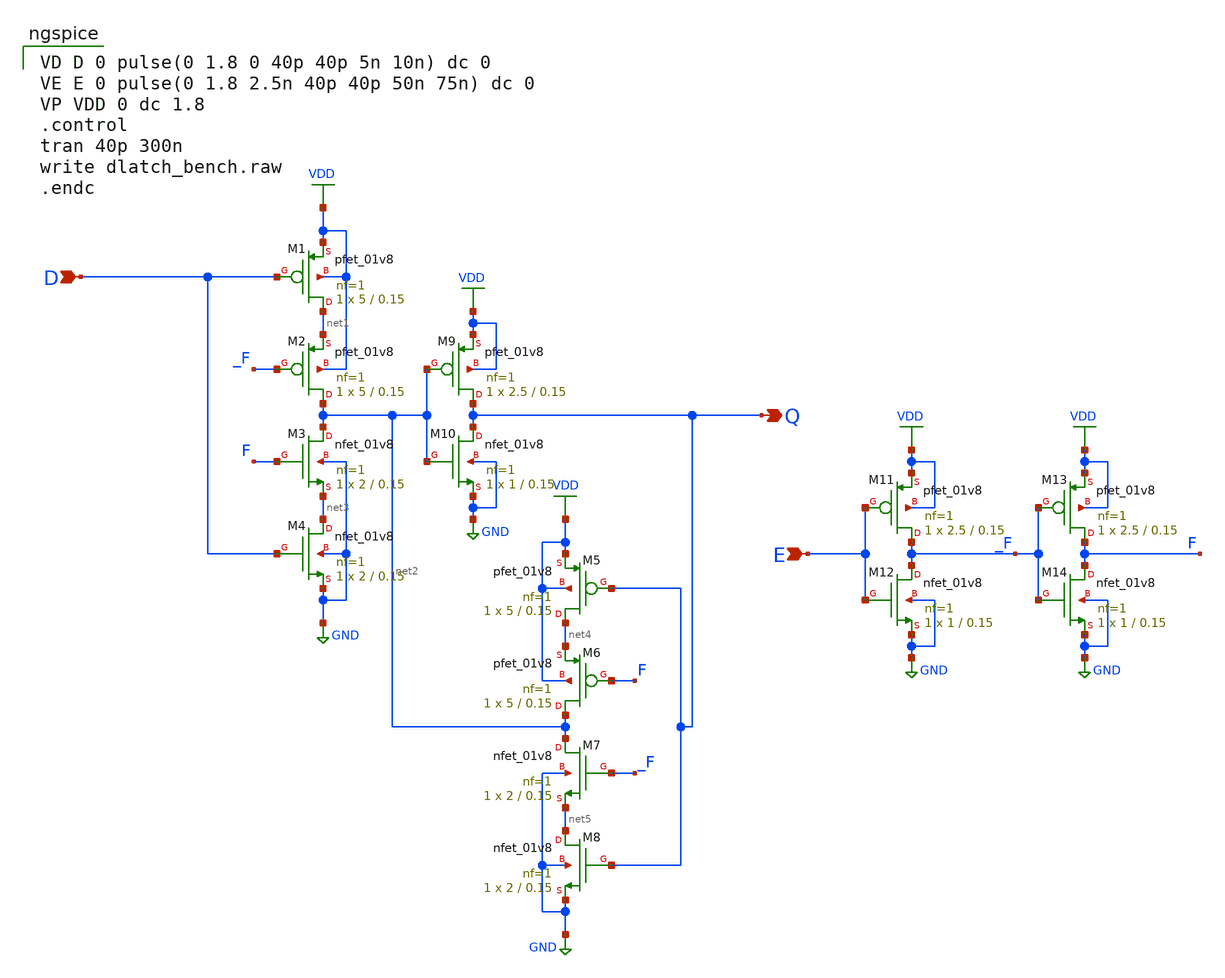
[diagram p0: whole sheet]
** sch_path: dlatch_bench2.sch
**.subckt dlatch_bench2 E D Q
*.ipin E
*.ipin D
*.opin Q
XM1 net1 D VDD VDD sky130_fd_pr__pfet_01v8 L=0.15 W=5 nf=1 ad='int((nf+1)/2) * W/nf * 0.29' as='int((nf+2)/2) * W/nf * 0.29'
+ pd='2*int((nf+1)/2) * (W/nf + 0.29)' ps='2*int((nf+2)/2) * (W/nf + 0.29)' nrd='0.29 / W' nrs='0.29 / W'
+ sa=0 sb=0 sd=0 mult=1 m=1
XM2 net2 _F net1 VDD sky130_fd_pr__pfet_01v8 L=0.15 W=5 nf=1 ad='int((nf+1)/2) * W/nf * 0.29' as='int((nf+2)/2) * W/nf * 0.29'
+ pd='2*int((nf+1)/2) * (W/nf + 0.29)' ps='2*int((nf+2)/2) * (W/nf + 0.29)' nrd='0.29 / W' nrs='0.29 / W'
+ sa=0 sb=0 sd=0 mult=1 m=1
XM3 net2 F net3 GND sky130_fd_pr__nfet_01v8 L=0.15 W=2 nf=1 ad='int((nf+1)/2) * W/nf * 0.29' as='int((nf+2)/2) * W/nf * 0.29'
+ pd='2*int((nf+1)/2) * (W/nf + 0.29)' ps='2*int((nf+2)/2) * (W/nf + 0.29)' nrd='0.29 / W' nrs='0.29 / W'
+ sa=0 sb=0 sd=0 mult=1 m=1
XM4 net3 D GND GND sky130_fd_pr__nfet_01v8 L=0.15 W=2 nf=1 ad='int((nf+1)/2) * W/nf * 0.29' as='int((nf+2)/2) * W/nf * 0.29'
+ pd='2*int((nf+1)/2) * (W/nf + 0.29)' ps='2*int((nf+2)/2) * (W/nf + 0.29)' nrd='0.29 / W' nrs='0.29 / W'
+ sa=0 sb=0 sd=0 mult=1 m=1
XM5 net4 Q VDD VDD sky130_fd_pr__pfet_01v8 L=0.15 W=5 nf=1 ad='int((nf+1)/2) * W/nf * 0.29' as='int((nf+2)/2) * W/nf * 0.29'
+ pd='2*int((nf+1)/2) * (W/nf + 0.29)' ps='2*int((nf+2)/2) * (W/nf + 0.29)' nrd='0.29 / W' nrs='0.29 / W'
+ sa=0 sb=0 sd=0 mult=1 m=1
XM6 net2 F net4 VDD sky130_fd_pr__pfet_01v8 L=0.15 W=5 nf=1 ad='int((nf+1)/2) * W/nf * 0.29' as='int((nf+2)/2) * W/nf * 0.29'
+ pd='2*int((nf+1)/2) * (W/nf + 0.29)' ps='2*int((nf+2)/2) * (W/nf + 0.29)' nrd='0.29 / W' nrs='0.29 / W'
+ sa=0 sb=0 sd=0 mult=1 m=1
XM7 net2 _F net5 GND sky130_fd_pr__nfet_01v8 L=0.15 W=2 nf=1 ad='int((nf+1)/2) * W/nf * 0.29' as='int((nf+2)/2) * W/nf * 0.29'
+ pd='2*int((nf+1)/2) * (W/nf + 0.29)' ps='2*int((nf+2)/2) * (W/nf + 0.29)' nrd='0.29 / W' nrs='0.29 / W'
+ sa=0 sb=0 sd=0 mult=1 m=1
XM8 net5 Q GND GND sky130_fd_pr__nfet_01v8 L=0.15 W=2 nf=1 ad='int((nf+1)/2) * W/nf * 0.29' as='int((nf+2)/2) * W/nf * 0.29'
+ pd='2*int((nf+1)/2) * (W/nf + 0.29)' ps='2*int((nf+2)/2) * (W/nf + 0.29)' nrd='0.29 / W' nrs='0.29 / W'
+ sa=0 sb=0 sd=0 mult=1 m=1
XM9 Q net2 VDD VDD sky130_fd_pr__pfet_01v8 L=0.15 W=2.5 nf=1 ad='int((nf+1)/2) * W/nf * 0.29' as='int((nf+2)/2) * W/nf * 0.29'
+ pd='2*int((nf+1)/2) * (W/nf + 0.29)' ps='2*int((nf+2)/2) * (W/nf + 0.29)' nrd='0.29 / W' nrs='0.29 / W'
+ sa=0 sb=0 sd=0 mult=1 m=1
XM10 Q net2 GND GND sky130_fd_pr__nfet_01v8 L=0.15 W=1 nf=1 ad='int((nf+1)/2) * W/nf * 0.29' as='int((nf+2)/2) * W/nf * 0.29'
+ pd='2*int((nf+1)/2) * (W/nf + 0.29)' ps='2*int((nf+2)/2) * (W/nf + 0.29)' nrd='0.29 / W' nrs='0.29 / W'
+ sa=0 sb=0 sd=0 mult=1 m=1
XM11 _F E VDD VDD sky130_fd_pr__pfet_01v8 L=0.15 W=2.5 nf=1 ad='int((nf+1)/2) * W/nf * 0.29' as='int((nf+2)/2) * W/nf * 0.29'
+ pd='2*int((nf+1)/2) * (W/nf + 0.29)' ps='2*int((nf+2)/2) * (W/nf + 0.29)' nrd='0.29 / W' nrs='0.29 / W'
+ sa=0 sb=0 sd=0 mult=1 m=1
XM12 _F E GND GND sky130_fd_pr__nfet_01v8 L=0.15 W=1 nf=1 ad='int((nf+1)/2) * W/nf * 0.29' as='int((nf+2)/2) * W/nf * 0.29'
+ pd='2*int((nf+1)/2) * (W/nf + 0.29)' ps='2*int((nf+2)/2) * (W/nf + 0.29)' nrd='0.29 / W' nrs='0.29 / W'
+ sa=0 sb=0 sd=0 mult=1 m=1
XM13 F _F VDD VDD sky130_fd_pr__pfet_01v8 L=0.15 W=2.5 nf=1 ad='int((nf+1)/2) * W/nf * 0.29' as='int((nf+2)/2) * W/nf * 0.29'
+ pd='2*int((nf+1)/2) * (W/nf + 0.29)' ps='2*int((nf+2)/2) * (W/nf + 0.29)' nrd='0.29 / W' nrs='0.29 / W'
+ sa=0 sb=0 sd=0 mult=1 m=1
XM14 F _F GND GND sky130_fd_pr__nfet_01v8 L=0.15 W=1 nf=1 ad='int((nf+1)/2) * W/nf * 0.29' as='int((nf+2)/2) * W/nf * 0.29'
+ pd='2*int((nf+1)/2) * (W/nf + 0.29)' ps='2*int((nf+2)/2) * (W/nf + 0.29)' nrd='0.29 / W' nrs='0.29 / W'
+ sa=0 sb=0 sd=0 mult=1 m=1
**** begin user architecture code

VD D 0 pulse(0 1.8 0 40p 40p 5n 10n) dc 0
VE E 0 pulse(0 1.8 2.5n 40p 40p 50n 75n) dc 0
VP VDD 0 dc 1.8
.control
tran 40p 300n
write dlatch_bench.raw
.endc


** opencircuitdesign pdks install
.lib $::SKYWATER_MODELS/sky130.lib.spice tt
.include $::SKYWATER_STDCELLS/sky130_fd_sc_hd.spice

**** end user architecture code
**.ends
.GLOBAL VDD
.GLOBAL GND
.end
